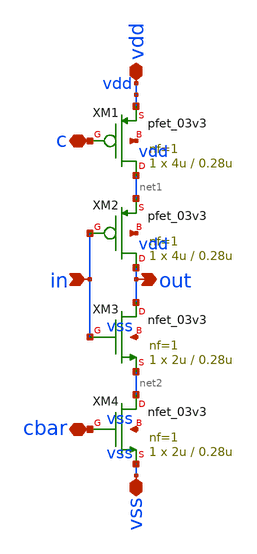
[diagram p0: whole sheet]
** sch_path: schematics/PC/TSI/TSI.sch
**.subckt TSI in out vdd vss cbar c
*.ipin in
*.opin out
*.iopin vdd
*.iopin vss
*.iopin cbar
*.iopin c
XM1 net1 c vdd vdd pfet_03v3 L=0.28u W=4u nf=1 ad='int((nf+1)/2) * W/nf * 0.18u' as='int((nf+2)/2) * W/nf * 0.18u'
+ pd='2*int((nf+1)/2) * (W/nf + 0.18u)' ps='2*int((nf+2)/2) * (W/nf + 0.18u)' nrd='0.18u / W' nrs='0.18u / W'
+ sa=0 sb=0 sd=0 m=1
XM2 out in net1 vdd pfet_03v3 L=0.28u W=4u nf=1 ad='int((nf+1)/2) * W/nf * 0.18u' as='int((nf+2)/2) * W/nf * 0.18u'
+ pd='2*int((nf+1)/2) * (W/nf + 0.18u)' ps='2*int((nf+2)/2) * (W/nf + 0.18u)' nrd='0.18u / W' nrs='0.18u / W'
+ sa=0 sb=0 sd=0 m=1
XM3 out in net2 vss nfet_03v3 L=0.28u W=2u nf=1 ad='int((nf+1)/2) * W/nf * 0.18u' as='int((nf+2)/2) * W/nf * 0.18u'
+ pd='2*int((nf+1)/2) * (W/nf + 0.18u)' ps='2*int((nf+2)/2) * (W/nf + 0.18u)' nrd='0.18u / W' nrs='0.18u / W'
+ sa=0 sb=0 sd=0 m=1
XM4 net2 cbar vss vss nfet_03v3 L=0.28u W=2u nf=1 ad='int((nf+1)/2) * W/nf * 0.18u' as='int((nf+2)/2) * W/nf * 0.18u'
+ pd='2*int((nf+1)/2) * (W/nf + 0.18u)' ps='2*int((nf+2)/2) * (W/nf + 0.18u)' nrd='0.18u / W' nrs='0.18u / W'
+ sa=0 sb=0 sd=0 m=1
**.ends
.end
